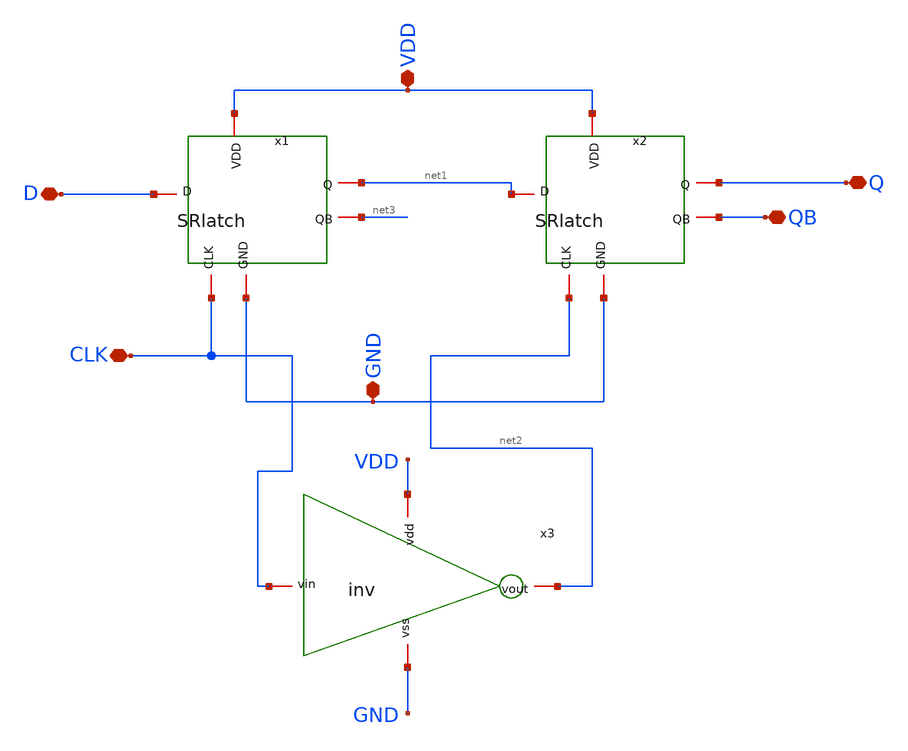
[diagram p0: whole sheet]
** sch_path: src/pixel/FF.sch
**.subckt FF Q VDD D CLK GND QB
*.iopin Q
*.iopin VDD
*.iopin D
*.iopin CLK
*.iopin GND
*.iopin QB
x1 D net1 GND CLK VDD net3 SRlatch
x2 net1 Q GND net2 VDD QB SRlatch
x3 VDD CLK net2 GND inv
**.ends
.end
